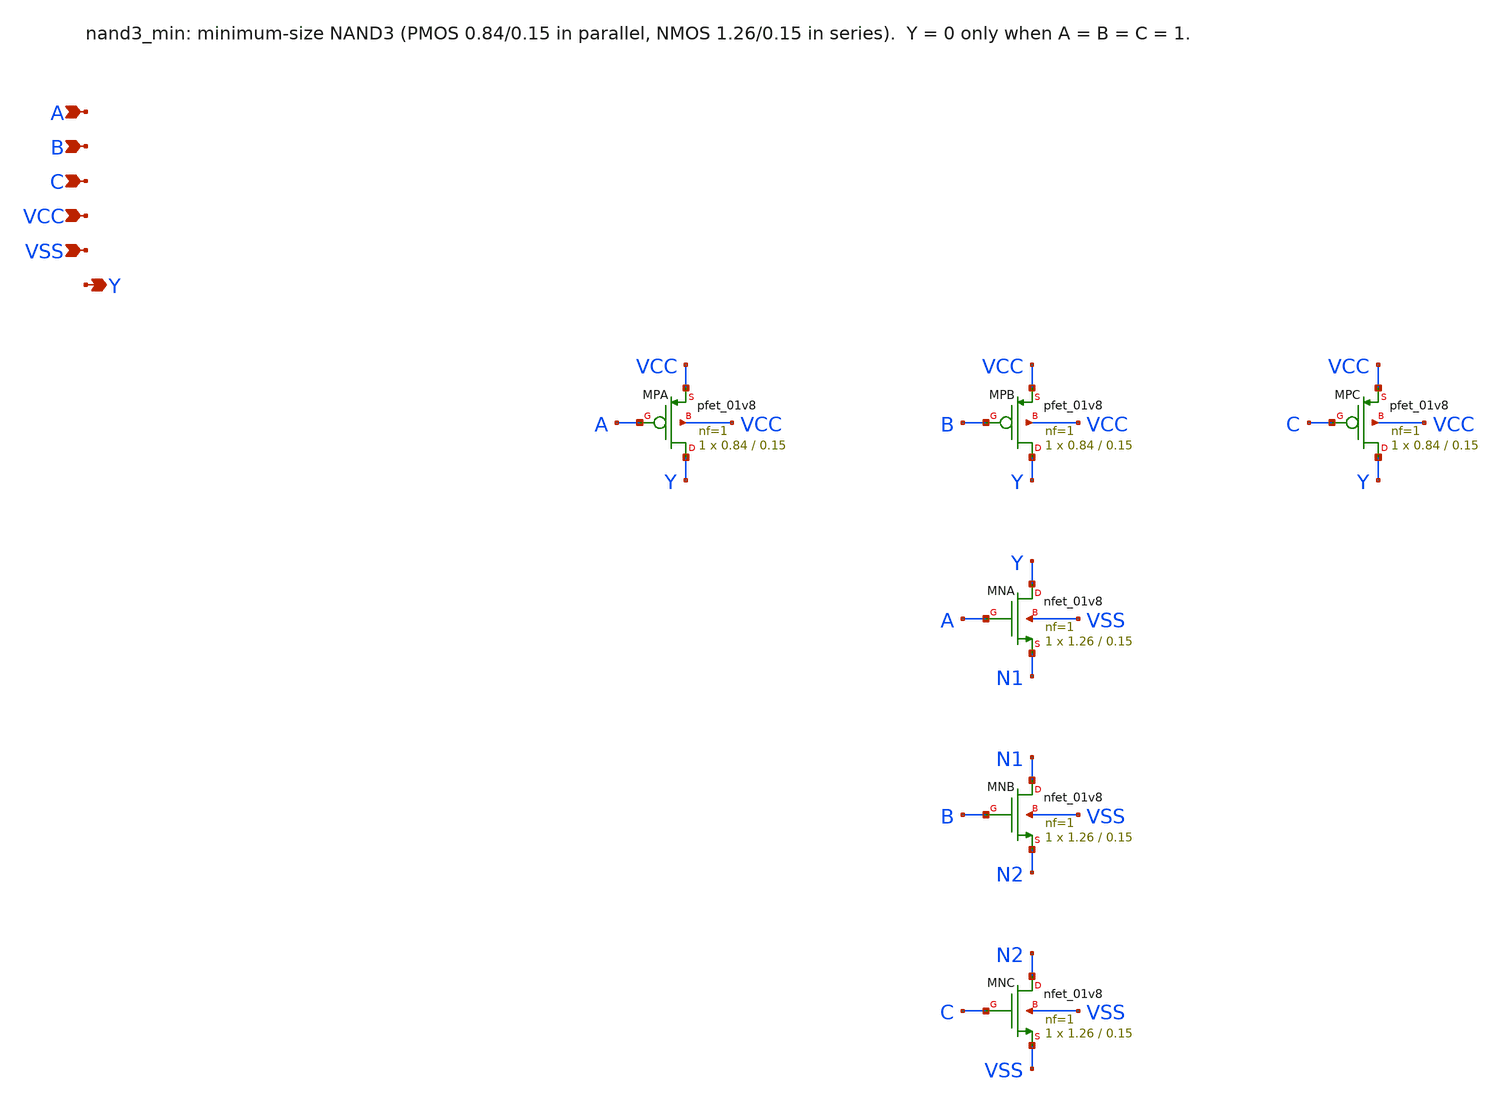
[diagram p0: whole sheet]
** sch_path: SAR_improved/nand3_min.sch
**.subckt nand3_min A B C VCC VSS Y
*.ipin A
*.ipin B
*.ipin C
*.ipin VCC
*.ipin VSS
*.opin Y
XMPA Y A VCC VCC sky130_fd_pr__pfet_01v8 L=0.15 W=0.84 nf=1 ad='int((nf+1)/2) * W/nf * 0.29' as='int((nf+2)/2) * W/nf * 0.29'
+ pd='2*int((nf+1)/2) * (W/nf + 0.29)' ps='2*int((nf+2)/2) * (W/nf + 0.29)' nrd='0.29 / W' nrs='0.29 / W'
+ sa=0 sb=0 sd=0 mult=1 m=1
XMPB Y B VCC VCC sky130_fd_pr__pfet_01v8 L=0.15 W=0.84 nf=1 ad='int((nf+1)/2) * W/nf * 0.29' as='int((nf+2)/2) * W/nf * 0.29'
+ pd='2*int((nf+1)/2) * (W/nf + 0.29)' ps='2*int((nf+2)/2) * (W/nf + 0.29)' nrd='0.29 / W' nrs='0.29 / W'
+ sa=0 sb=0 sd=0 mult=1 m=1
XMPC Y C VCC VCC sky130_fd_pr__pfet_01v8 L=0.15 W=0.84 nf=1 ad='int((nf+1)/2) * W/nf * 0.29' as='int((nf+2)/2) * W/nf * 0.29'
+ pd='2*int((nf+1)/2) * (W/nf + 0.29)' ps='2*int((nf+2)/2) * (W/nf + 0.29)' nrd='0.29 / W' nrs='0.29 / W'
+ sa=0 sb=0 sd=0 mult=1 m=1
XMNA Y A N1 VSS sky130_fd_pr__nfet_01v8 L=0.15 W=1.26 nf=1 ad='int((nf+1)/2) * W/nf * 0.29' as='int((nf+2)/2) * W/nf * 0.29'
+ pd='2*int((nf+1)/2) * (W/nf + 0.29)' ps='2*int((nf+2)/2) * (W/nf + 0.29)' nrd='0.29 / W' nrs='0.29 / W'
+ sa=0 sb=0 sd=0 mult=1 m=1
XMNB N1 B N2 VSS sky130_fd_pr__nfet_01v8 L=0.15 W=1.26 nf=1 ad='int((nf+1)/2) * W/nf * 0.29' as='int((nf+2)/2) * W/nf * 0.29'
+ pd='2*int((nf+1)/2) * (W/nf + 0.29)' ps='2*int((nf+2)/2) * (W/nf + 0.29)' nrd='0.29 / W' nrs='0.29 / W'
+ sa=0 sb=0 sd=0 mult=1 m=1
XMNC N2 C VSS VSS sky130_fd_pr__nfet_01v8 L=0.15 W=1.26 nf=1 ad='int((nf+1)/2) * W/nf * 0.29' as='int((nf+2)/2) * W/nf * 0.29'
+ pd='2*int((nf+1)/2) * (W/nf + 0.29)' ps='2*int((nf+2)/2) * (W/nf + 0.29)' nrd='0.29 / W' nrs='0.29 / W'
+ sa=0 sb=0 sd=0 mult=1 m=1
**.ends
.end
